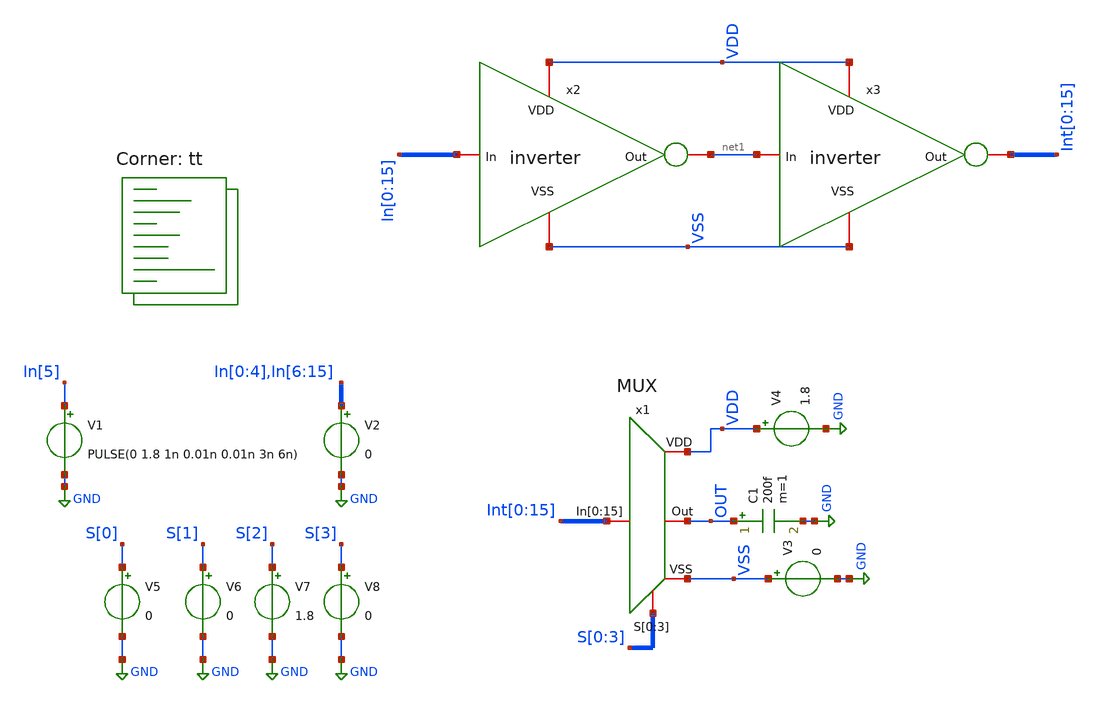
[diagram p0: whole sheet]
** sch_path: MUX/TB_MUX.sch
**.subckt TB_MUX
x1 VDD VSS Int[0] Int[1] Int[2] Int[3] Int[4] Int[5] Int[6] Int[7] Int[8] Int[9] Int[10] Int[11]
+ Int[12] Int[13] Int[14] Int[15] OUT S[0] S[1] S[2] S[3] MUX
V1 In[5] GND PULSE(0 1.8 1n 0.01n 0.01n 3n 6n)
V4 VDD GND 1.8
V5 S[0] GND 0
V6 S[1] GND 0
V7 S[2] GND 1.8
V8 S[3] GND 0
V2 In[0] GND 0
V3 VSS GND 0
C1 OUT GND 200f m=1
x2 VDD net1 In[0] VSS inverter
x3 VDD Int[0] net1 VSS inverter
**** begin user architecture code


.ic V(In[0:15])=0
.tran 0.01n 4n
.save all


.lib $::SKYWATER_MODELS/sky130.lib.spice tt
**** end user architecture code
**.ends

* expanding   symbol:  MUX.sym # of pins=5
** sym_path: MUX/MUX.sym
** sch_path: MUX/MUX.sch
.subckt MUX VDD VSS In[0] In[1] In[2] In[3] In[4] In[5] In[6] In[7] In[8] In[9] In[10] In[11] In[12]
+ In[13] In[14] In[15] Out S[0] S[1] S[2] S[3]
*.iopin VDD
*.iopin VSS
*.iopin
*+ In[0],In[1],In[2],In[3],In[4],In[5],In[6],In[7],In[8],In[9],In[10],In[11],In[12],In[13],In[14],In[15]
*.iopin Out
*.iopin S[0],S[1],S[2],S[3]
X[0] S[0] VDD R0[0] In[0] VSS S[0]B MUX_TG
x1 VDD S[0]B S[0] VSS inverter
X[13] S[1] VDD R1[0] R0[0] VSS S[1]B MUX_TG
x2 VDD S[1]B S[1] VSS inverter
X[19] S[2] VDD R3[0] R1[0] VSS S[2]B MUX_TG
x3 VDD S[2]B S[2] VSS inverter
x4 VDD S[3]B S[3] VSS inverter
X[22] S[3] VDD Out R3[0] VSS S[3]B MUX_TG
X[1] S[0]B VDD R0[0] In[1] VSS S[0] MUX_TG
X[14] S[1]B VDD R1[0] R0[1] VSS S[1] MUX_TG
X[20] S[2]B VDD R3[0] R1[1] VSS S[2] MUX_TG
X[23] S[3]B VDD Out R3[1] VSS S[3] MUX_TG
X[2] S[0] VDD R0[1] In[2] VSS S[0]B MUX_TG
X[15] S[1] VDD R1[1] R0[2] VSS S[1]B MUX_TG
X[21] S[2] VDD R3[1] R1[2] VSS S[2]B MUX_TG
X[3] S[0]B VDD R0[1] In[3] VSS S[0] MUX_TG
X[16] S[1]B VDD R1[1] R0[3] VSS S[1] MUX_TG
X[4] S[0] VDD R0[2] In[4] VSS S[0]B MUX_TG
X[17] S[1] VDD R1[2] R0[4] VSS S[1]B MUX_TG
X[5] S[0]B VDD R0[2] In[5] VSS S[0] MUX_TG
X[18] S[1]B VDD R1[2] R0[5] VSS S[1] MUX_TG
X[6] S[0] VDD R0[3] In[6] VSS S[0]B MUX_TG
X[7] S[0]B VDD R0[3] In[7] VSS S[0] MUX_TG
X[8] S[0] VDD R0[4] In[8] VSS S[0]B MUX_TG
X[9] S[0]B VDD R0[4] In[9] VSS S[0] MUX_TG
X[10] S[0] VDD R0[5] In[10] VSS S[0]B MUX_TG
X[11] S[0]B VDD R0[5] In[11] VSS S[0] MUX_TG
.ends


* expanding   symbol:  inverter.sym # of pins=4
** sym_path: MUX/inverter.sym
** sch_path: MUX/inverter.sch
.subckt inverter VDD Out In VSS
*.iopin VDD
*.iopin Out
*.iopin VSS
*.iopin In
XM3 Out In VSS VSS sky130_fd_pr__nfet_01v8 L=0.15 W=2.1 nf=1 ad='int((nf+1)/2) * W/nf * 0.29' as='int((nf+2)/2) * W/nf * 0.29'
+ pd='2*int((nf+1)/2) * (W/nf + 0.29)' ps='2*int((nf+2)/2) * (W/nf + 0.29)' nrd='0.29 / W' nrs='0.29 / W'
+ sa=0 sb=0 sd=0 mult=2 m=2
XM1 Out In VDD VDD sky130_fd_pr__pfet_01v8 L=0.15 W=4.75 nf=1 ad='int((nf+1)/2) * W/nf * 0.29' as='int((nf+2)/2) * W/nf * 0.29'
+ pd='2*int((nf+1)/2) * (W/nf + 0.29)' ps='2*int((nf+2)/2) * (W/nf + 0.29)' nrd='0.29 / W' nrs='0.29 / W'
+ sa=0 sb=0 sd=0 mult=4 m=4
.ends


* expanding   symbol:  MUX_TG.sym # of pins=6
** sym_path: MUX/MUX_TG.sym
** sch_path: MUX/MUX_TG.sch
.subckt MUX_TG AB VDD Out In VSS A
*.iopin In
*.iopin Out
*.iopin VDD
*.iopin VSS
*.iopin AB
*.iopin A
XM1 In A Out VSS sky130_fd_pr__nfet_01v8 L=0.15 W=2.1 nf=1 ad='int((nf+1)/2) * W/nf * 0.29' as='int((nf+2)/2) * W/nf * 0.29'
+ pd='2*int((nf+1)/2) * (W/nf + 0.29)' ps='2*int((nf+2)/2) * (W/nf + 0.29)' nrd='0.29 / W' nrs='0.29 / W'
+ sa=0 sb=0 sd=0 mult=2 m=2
XM2 In AB Out VDD sky130_fd_pr__pfet_01v8 L=0.15 W=4.75 nf=1 ad='int((nf+1)/2) * W/nf * 0.29' as='int((nf+2)/2) * W/nf * 0.29'
+ pd='2*int((nf+1)/2) * (W/nf + 0.29)' ps='2*int((nf+2)/2) * (W/nf + 0.29)' nrd='0.29 / W' nrs='0.29 / W'
+ sa=0 sb=0 sd=0 mult=4 m=4
.ends

.GLOBAL GND
.end
